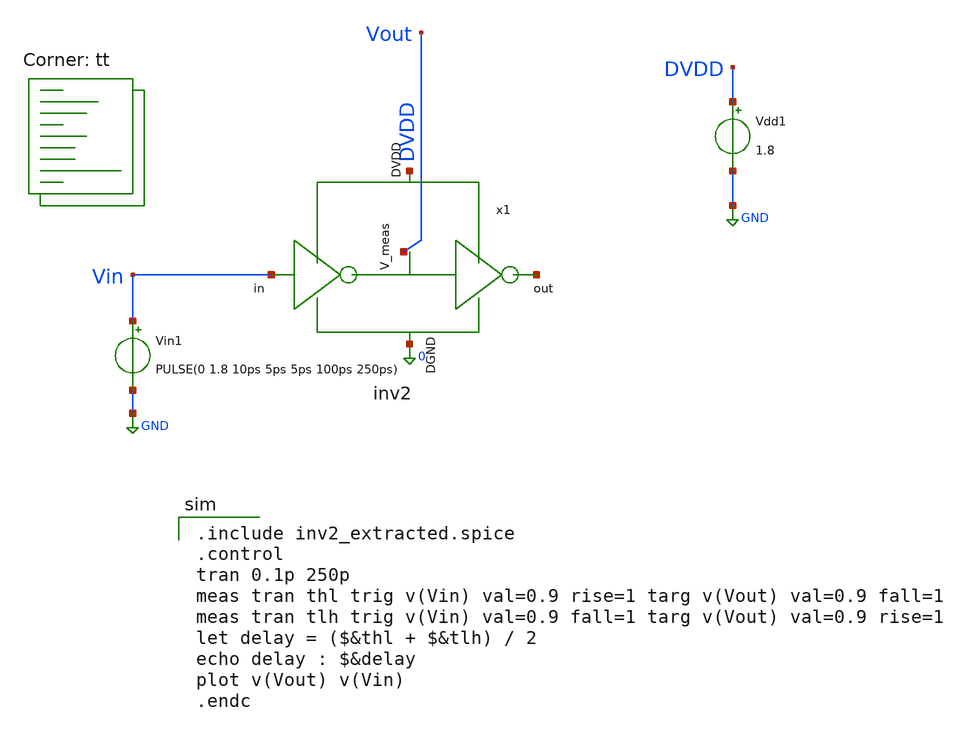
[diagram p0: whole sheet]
** sch_path: tutorial-4/source/q1b/q1b.sch
**.subckt q1b
Vin1 Vin GND PULSE(0 1.8 10ps 5ps 5ps 100ps 250ps)
Vdd1 DVDD GND 1.8
x1 DVDD net1 Vout Vin 0 inv2
**** begin user architecture code
.lib $::SKYWATER_MODELS/sky130.lib.spice tt

.include inv2_extracted.spice
.control
tran 0.1p 250p
meas tran thl trig v(Vin) val=0.9 rise=1 targ v(Vout) val=0.9 fall=1
meas tran tlh trig v(Vin) val=0.9 fall=1 targ v(Vout) val=0.9 rise=1
let delay = ($&thl + $&tlh) / 2
echo delay : $&delay
plot v(Vout) v(Vin)
.endc

**** end user architecture code
**.ends
.GLOBAL GND
.end
